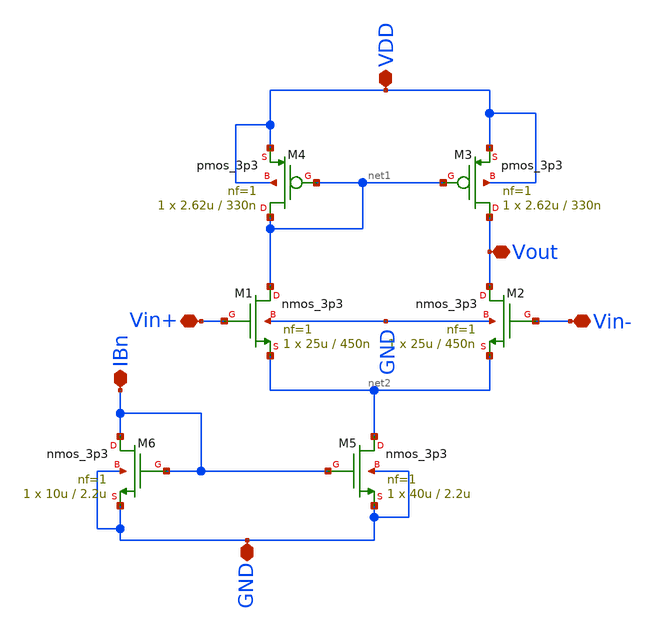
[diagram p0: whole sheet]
** sch_path: ITI_Labs/Lab7/Design/Lab07.sch
**.subckt Lab07 VDD GND IBn Vin- Vin+ Vout
*.iopin VDD
*.iopin GND
*.iopin IBn
*.iopin Vin-
*.iopin Vin+
*.iopin Vout
XM1 net1 Vin+ net2 GND nmos_3p3 L=450n W=25u nf=1 ad='int((nf+1)/2) * W/nf * 0.18u' as='int((nf+2)/2) * W/nf * 0.18u'
+ pd='2*int((nf+1)/2) * (W/nf + 0.18u)' ps='2*int((nf+2)/2) * (W/nf + 0.18u)' nrd='0.18u / W' nrs='0.18u / W'
+ sa=0 sb=0 sd=0 m=1
XM4 net1 net1 VDD VDD pmos_3p3 L=330n W=2.62u nf=1 ad='int((nf+1)/2) * W/nf * 0.18u' as='int((nf+2)/2) * W/nf * 0.18u'
+ pd='2*int((nf+1)/2) * (W/nf + 0.18u)' ps='2*int((nf+2)/2) * (W/nf + 0.18u)' nrd='0.18u / W' nrs='0.18u / W'
+ sa=0 sb=0 sd=0 m=1
XM5 net2 IBn GND GND nmos_3p3 L=2.2u W=40u nf=1 ad='int((nf+1)/2) * W/nf * 0.18u' as='int((nf+2)/2) * W/nf * 0.18u'
+ pd='2*int((nf+1)/2) * (W/nf + 0.18u)' ps='2*int((nf+2)/2) * (W/nf + 0.18u)' nrd='0.18u / W' nrs='0.18u / W'
+ sa=0 sb=0 sd=0 m=1
XM2 Vout Vin- net2 GND nmos_3p3 L=450n W=25u nf=1 ad='int((nf+1)/2) * W/nf * 0.18u' as='int((nf+2)/2) * W/nf * 0.18u'
+ pd='2*int((nf+1)/2) * (W/nf + 0.18u)' ps='2*int((nf+2)/2) * (W/nf + 0.18u)' nrd='0.18u / W' nrs='0.18u / W'
+ sa=0 sb=0 sd=0 m=1
XM3 Vout net1 VDD VDD pmos_3p3 L=330n W=2.62u nf=1 ad='int((nf+1)/2) * W/nf * 0.18u' as='int((nf+2)/2) * W/nf * 0.18u'
+ pd='2*int((nf+1)/2) * (W/nf + 0.18u)' ps='2*int((nf+2)/2) * (W/nf + 0.18u)' nrd='0.18u / W' nrs='0.18u / W'
+ sa=0 sb=0 sd=0 m=1
XM6 IBn IBn GND GND nmos_3p3 L=2.2u W=10u nf=1 ad='int((nf+1)/2) * W/nf * 0.18u' as='int((nf+2)/2) * W/nf * 0.18u'
+ pd='2*int((nf+1)/2) * (W/nf + 0.18u)' ps='2*int((nf+2)/2) * (W/nf + 0.18u)' nrd='0.18u / W' nrs='0.18u / W'
+ sa=0 sb=0 sd=0 m=1
**.ends
.end
